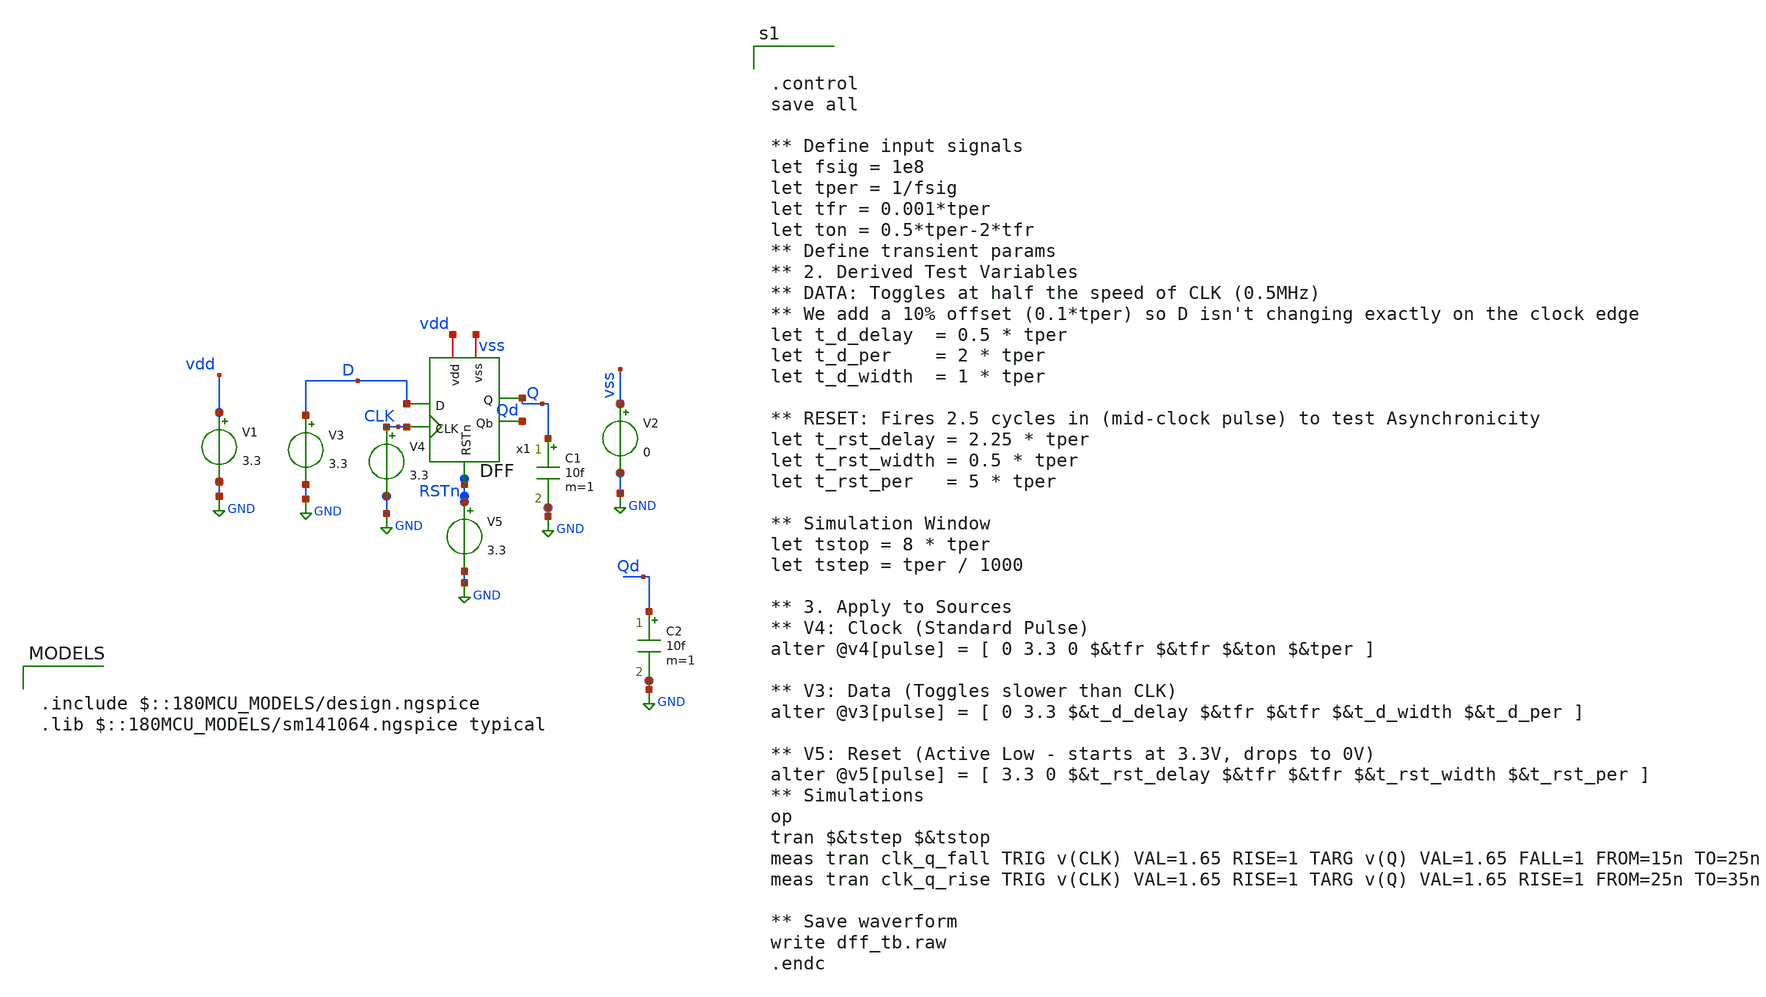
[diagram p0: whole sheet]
** sch_path: schematics/PC/DFF/DFF_tb.sch
**.subckt DFF_tb
V2 vss GND 0
V1 vdd GND 3.3
V3 D GND 3.3
V4 CLK GND 3.3
V5 RSTn GND 3.3
C1 Q GND 10f m=1
C2 Qd GND 10f m=1
x1 vdd RSTn D Q Qd CLK vss DFF
**** begin user architecture code

.include $::180MCU_MODELS/design.ngspice
.lib $::180MCU_MODELS/sm141064.ngspice typical



.control
save all

** Define input signals
let fsig = 1e8
let tper = 1/fsig
let tfr = 0.001*tper
let ton = 0.5*tper-2*tfr
** Define transient params
** 2. Derived Test Variables
** DATA: Toggles at half the speed of CLK (0.5MHz)
** We add a 10% offset (0.1*tper) so D isn't changing exactly on the clock edge
let t_d_delay  = 0.5 * tper
let t_d_per    = 2 * tper
let t_d_width  = 1 * tper

** RESET: Fires 2.5 cycles in (mid-clock pulse) to test Asynchronicity
let t_rst_delay = 2.25 * tper
let t_rst_width = 0.5 * tper
let t_rst_per   = 5 * tper

** Simulation Window
let tstop = 8 * tper
let tstep = tper / 1000

** 3. Apply to Sources
** V4: Clock (Standard Pulse)
alter @v4[pulse] = [ 0 3.3 0 $&tfr $&tfr $&ton $&tper ]

** V3: Data (Toggles slower than CLK)
alter @v3[pulse] = [ 0 3.3 $&t_d_delay $&tfr $&tfr $&t_d_width $&t_d_per ]

** V5: Reset (Active Low - starts at 3.3V, drops to 0V)
alter @v5[pulse] = [ 3.3 0 $&t_rst_delay $&tfr $&tfr $&t_rst_width $&t_rst_per ]
** Simulations
op
tran $&tstep $&tstop
meas tran clk_q_fall TRIG v(CLK) VAL=1.65 RISE=1 TARG v(Q) VAL=1.65 FALL=1 FROM=15n TO=25n
meas tran clk_q_rise TRIG v(CLK) VAL=1.65 RISE=1 TARG v(Q) VAL=1.65 RISE=1 FROM=25n TO=35n

** Save waverform
write dff_tb.raw
.endc



**** end user architecture code
**.ends
.GLOBAL GND
.end
